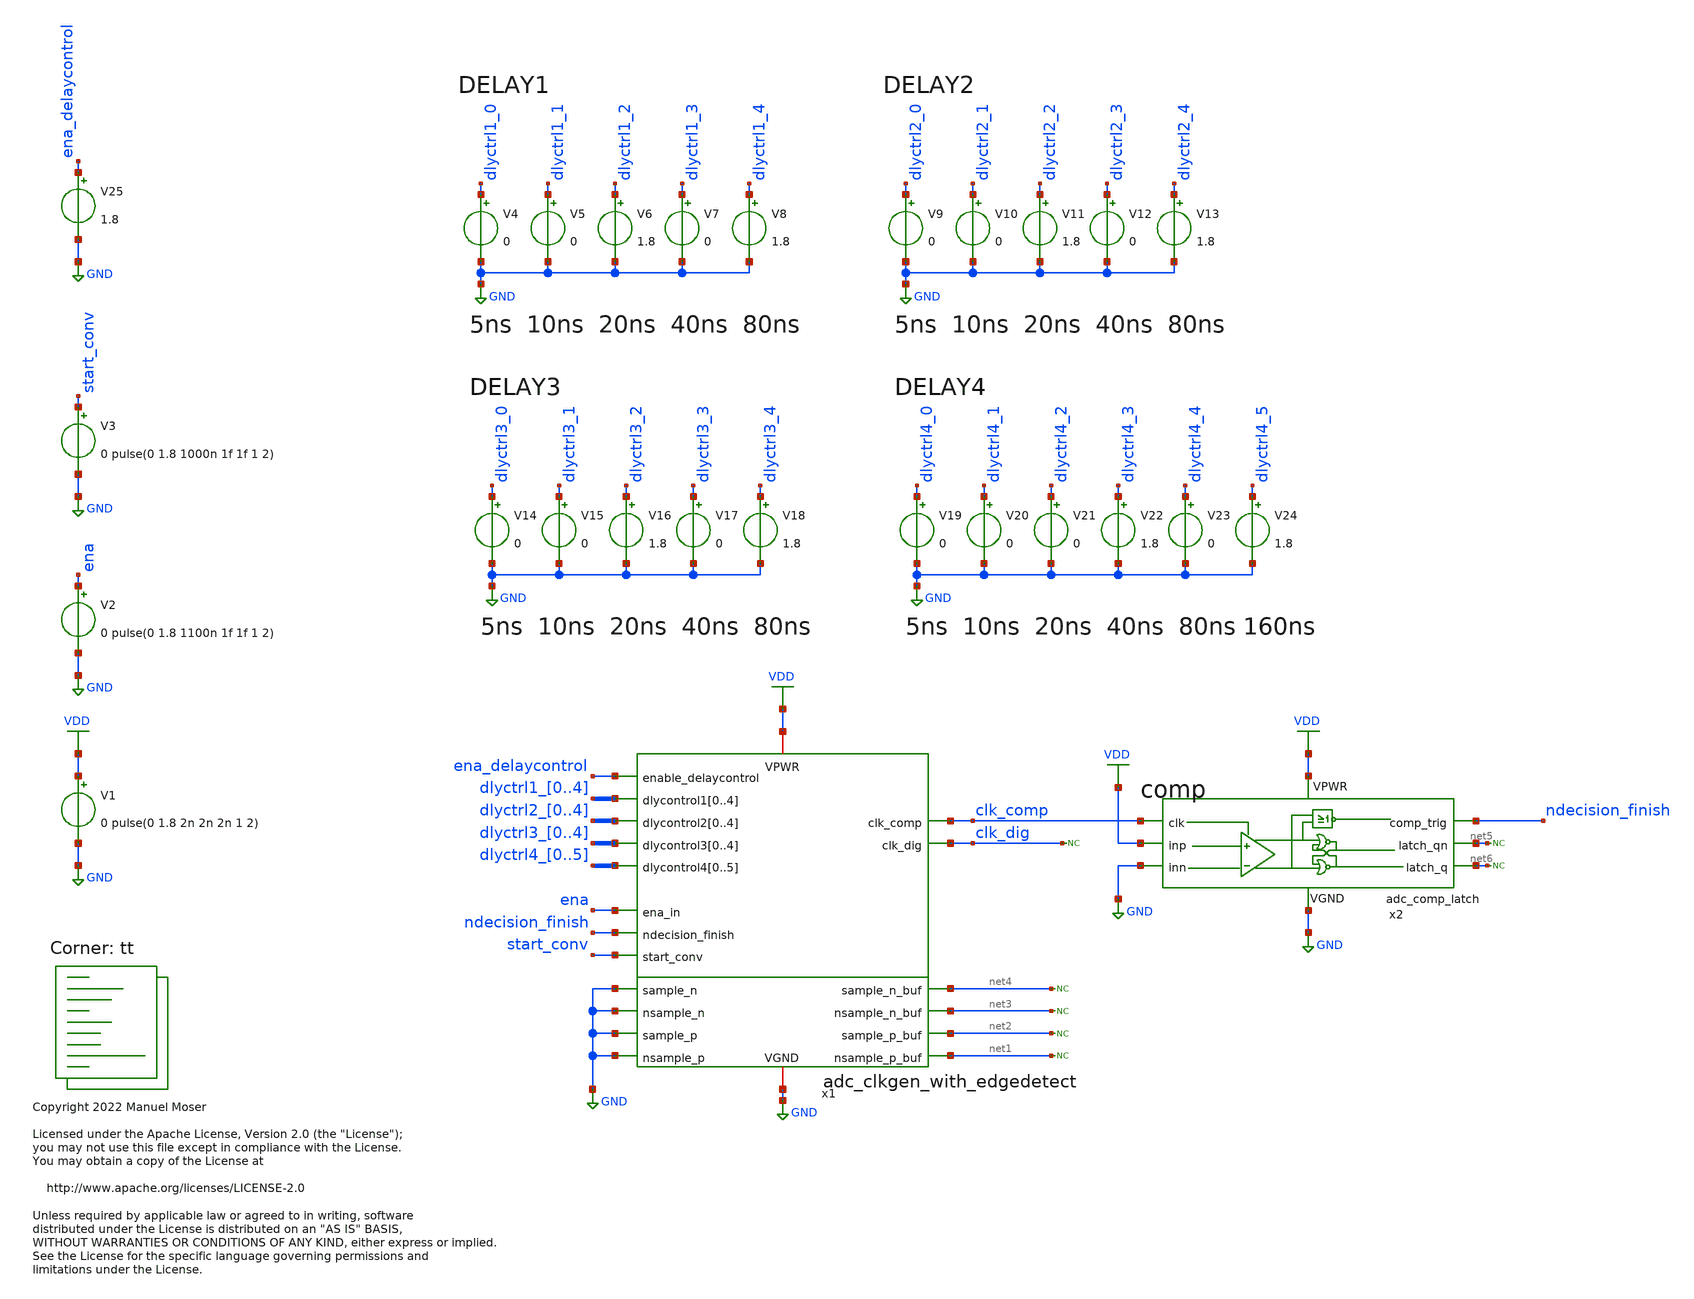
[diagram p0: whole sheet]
** sch_path: openlane/adc_clkgen_with_edgedetect/validation/adc_clkgen_with_edgedetect_tb.sch
* Copyright 2022 Manuel Moser
* Licensed under the Apache License, Version 2.0 (the "License");
**.subckt adc_clkgen_with_edgedetect_tb
x1 GND VDD clk_comp clk_dig dlyctrl1_0 dlyctrl1_1 dlyctrl1_2 dlyctrl1_3 dlyctrl1_4 dlyctrl2_0
+ dlyctrl2_1 dlyctrl2_2 dlyctrl2_3 dlyctrl2_4 dlyctrl3_0 dlyctrl3_1 dlyctrl3_2 dlyctrl3_3 dlyctrl3_4 dlyctrl4_0
+ dlyctrl4_1 dlyctrl4_2 dlyctrl4_3 dlyctrl4_4 dlyctrl4_5 ena ena_delaycontrol ndecision_finish GND net3 GND net1
+ GND net4 GND net2 start_conv adc_clkgen_with_edgedetect
V1 VDD GND 0 pulse(0 1.8 2n 2n 2n 1 2)
* noconn clk_dig
* noconn #net4
* noconn #net3
* noconn #net2
* noconn #net1
V2 ena GND 0 pulse(0 1.8 1100n 1f 1f 1 2)
V3 start_conv GND 0 pulse(0 1.8 1000n 1f 1f 1 2)
V4 dlyctrl1_0 GND 0
V5 dlyctrl1_1 GND 0
V6 dlyctrl1_2 GND 1.8
V7 dlyctrl1_3 GND 0
V8 dlyctrl1_4 GND 1.8
V9 dlyctrl2_0 GND 0
V10 dlyctrl2_1 GND 0
V11 dlyctrl2_2 GND 1.8
V12 dlyctrl2_3 GND 0
V13 dlyctrl2_4 GND 1.8
V14 dlyctrl3_0 GND 0
V15 dlyctrl3_1 GND 0
V16 dlyctrl3_2 GND 1.8
V17 dlyctrl3_3 GND 0
V18 dlyctrl3_4 GND 1.8
V19 dlyctrl4_0 GND 0
V20 dlyctrl4_1 GND 0
V21 dlyctrl4_2 GND 0
V22 dlyctrl4_3 GND 1.8
V23 dlyctrl4_4 GND 0
V24 dlyctrl4_5 GND 1.8
V25 ena_delaycontrol GND 1.8
x2 VDD GND clk_comp VDD GND ndecision_finish net5 net6 adc_comp_latch
* noconn #net5
* noconn #net6
**** begin user architecture code


.include /foss/designs/SKY130_SAR-ADC/openlane/adc_clkgen_with_edgedetect/validation/adc_clkgen_with_edgedetect.spice
*.OPTIONS RELTOL=.001 TRTOL=1 ABSTOL=1e-16 CHGTOL=1.0e-16 DEFAD=1.0e-16
.save all
.control
tran 100p 3600n
plot v(clk_comp) v(ndecision_finish) v(clk_dig)
.endc

.lib $::SKYWATER_MODELS/sky130.lib.spice tt
**** end user architecture code
**.ends
.GLOBAL GND
.GLOBAL VDD
.end
